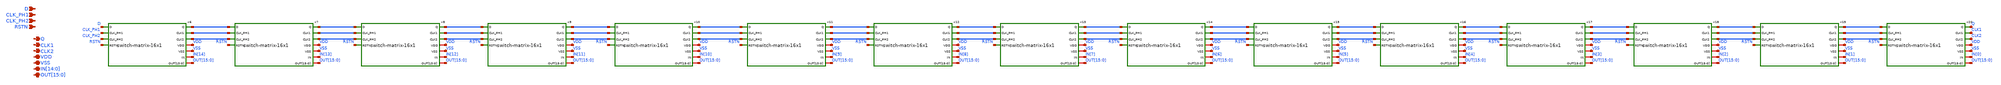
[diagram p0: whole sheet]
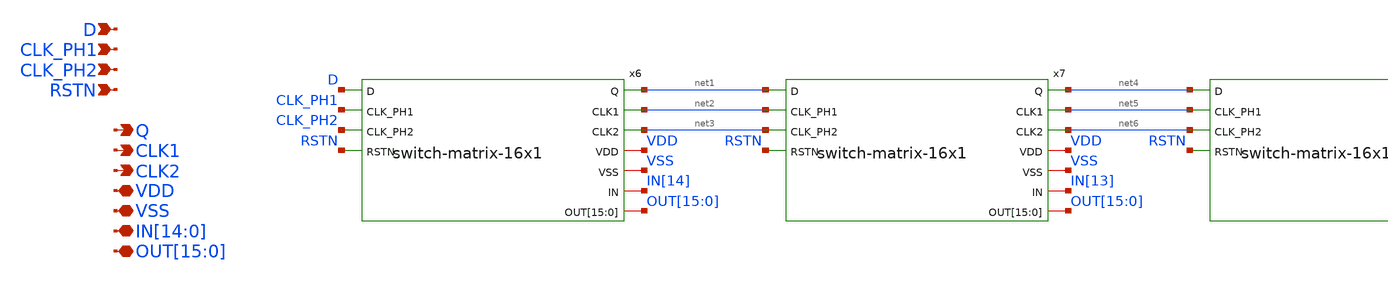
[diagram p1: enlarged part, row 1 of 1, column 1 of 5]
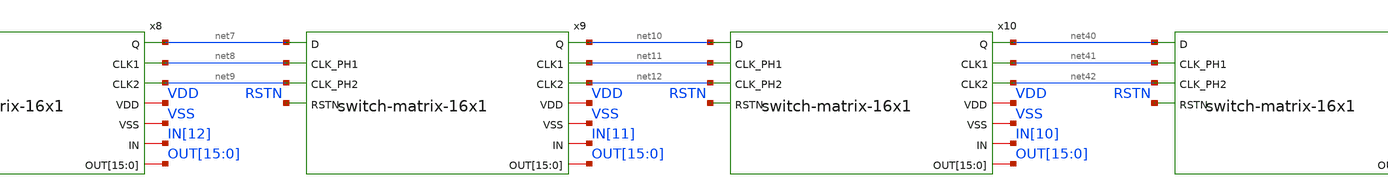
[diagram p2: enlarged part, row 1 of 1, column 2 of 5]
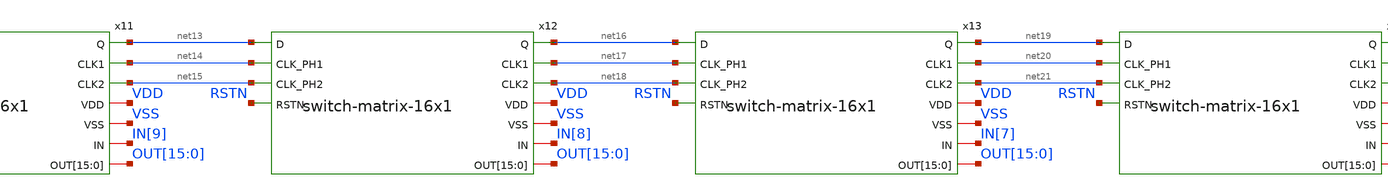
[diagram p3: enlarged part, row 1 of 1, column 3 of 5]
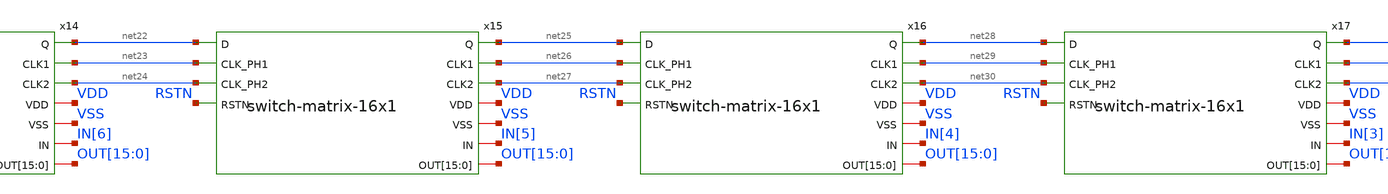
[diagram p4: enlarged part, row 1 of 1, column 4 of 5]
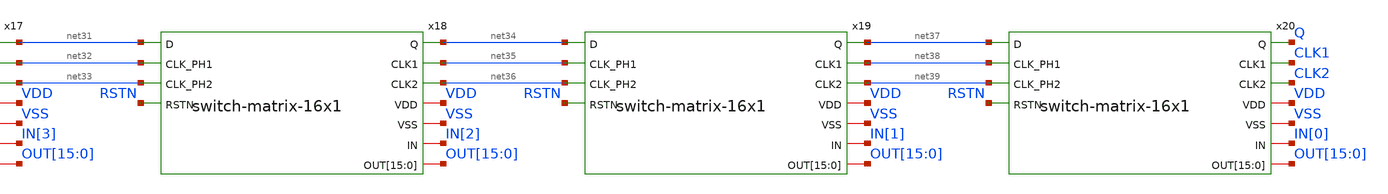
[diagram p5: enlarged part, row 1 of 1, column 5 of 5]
** sch_path: designs/libs/core_switch-matrix/switch-matrix-16x20/switch-matrix-16x20.sch
**.subckt switch-matrix-16x20 D CLK_PH1 CLK_PH2 RSTN VDD VSS
*+ IN[14],IN[13],IN[12],IN[11],IN[10],IN[9],IN[8],IN[7],IN[6],IN[5],IN[4],IN[3],IN[2],IN[1],IN[0]
*+ OUT[15],OUT[14],OUT[13],OUT[12],OUT[11],OUT[10],OUT[9],OUT[8],OUT[7],OUT[6],OUT[5],OUT[4],OUT[3],OUT[2],OUT[1],OUT[0] Q CLK1 CLK2
*.ipin D
*.ipin CLK_PH1
*.ipin CLK_PH2
*.ipin RSTN
*.iopin VDD
*.iopin VSS
*.iopin
*+ IN[14],IN[13],IN[12],IN[11],IN[10],IN[9],IN[8],IN[7],IN[6],IN[5],IN[4],IN[3],IN[2],IN[1],IN[0]
*.iopin
*+ OUT[15],OUT[14],OUT[13],OUT[12],OUT[11],OUT[10],OUT[9],OUT[8],OUT[7],OUT[6],OUT[5],OUT[4],OUT[3],OUT[2],OUT[1],OUT[0]
*.opin Q
*.opin CLK1
*.opin CLK2
x6 net1 net2 net3 VDD VSS IN[14] OUT[15] OUT[14] OUT[13] OUT[12] OUT[11] OUT[10] OUT[9] OUT[8]
+ OUT[7] OUT[6] OUT[5] OUT[4] OUT[3] OUT[2] OUT[1] OUT[0] D CLK_PH1 CLK_PH2 RSTN switch-matrix-16x1
x7 net4 net5 net6 VDD VSS IN[13] OUT[15] OUT[14] OUT[13] OUT[12] OUT[11] OUT[10] OUT[9] OUT[8]
+ OUT[7] OUT[6] OUT[5] OUT[4] OUT[3] OUT[2] OUT[1] OUT[0] net1 net2 net3 RSTN switch-matrix-16x1
x8 net7 net8 net9 VDD VSS IN[12] OUT[15] OUT[14] OUT[13] OUT[12] OUT[11] OUT[10] OUT[9] OUT[8]
+ OUT[7] OUT[6] OUT[5] OUT[4] OUT[3] OUT[2] OUT[1] OUT[0] net4 net5 net6 RSTN switch-matrix-16x1
x9 net10 net11 net12 VDD VSS IN[11] OUT[15] OUT[14] OUT[13] OUT[12] OUT[11] OUT[10] OUT[9] OUT[8]
+ OUT[7] OUT[6] OUT[5] OUT[4] OUT[3] OUT[2] OUT[1] OUT[0] net7 net8 net9 RSTN switch-matrix-16x1
x10 net40 net41 net42 VDD VSS IN[10] OUT[15] OUT[14] OUT[13] OUT[12] OUT[11] OUT[10] OUT[9] OUT[8]
+ OUT[7] OUT[6] OUT[5] OUT[4] OUT[3] OUT[2] OUT[1] OUT[0] net10 net11 net12 RSTN switch-matrix-16x1
x11 net13 net14 net15 VDD VSS IN[9] OUT[15] OUT[14] OUT[13] OUT[12] OUT[11] OUT[10] OUT[9] OUT[8]
+ OUT[7] OUT[6] OUT[5] OUT[4] OUT[3] OUT[2] OUT[1] OUT[0] net40 net41 net42 RSTN switch-matrix-16x1
x12 net16 net17 net18 VDD VSS IN[8] OUT[15] OUT[14] OUT[13] OUT[12] OUT[11] OUT[10] OUT[9] OUT[8]
+ OUT[7] OUT[6] OUT[5] OUT[4] OUT[3] OUT[2] OUT[1] OUT[0] net13 net14 net15 RSTN switch-matrix-16x1
x13 net19 net20 net21 VDD VSS IN[7] OUT[15] OUT[14] OUT[13] OUT[12] OUT[11] OUT[10] OUT[9] OUT[8]
+ OUT[7] OUT[6] OUT[5] OUT[4] OUT[3] OUT[2] OUT[1] OUT[0] net16 net17 net18 RSTN switch-matrix-16x1
x14 net22 net23 net24 VDD VSS IN[6] OUT[15] OUT[14] OUT[13] OUT[12] OUT[11] OUT[10] OUT[9] OUT[8]
+ OUT[7] OUT[6] OUT[5] OUT[4] OUT[3] OUT[2] OUT[1] OUT[0] net19 net20 net21 RSTN switch-matrix-16x1
x15 net25 net26 net27 VDD VSS IN[5] OUT[15] OUT[14] OUT[13] OUT[12] OUT[11] OUT[10] OUT[9] OUT[8]
+ OUT[7] OUT[6] OUT[5] OUT[4] OUT[3] OUT[2] OUT[1] OUT[0] net22 net23 net24 RSTN switch-matrix-16x1
x16 net28 net29 net30 VDD VSS IN[4] OUT[15] OUT[14] OUT[13] OUT[12] OUT[11] OUT[10] OUT[9] OUT[8]
+ OUT[7] OUT[6] OUT[5] OUT[4] OUT[3] OUT[2] OUT[1] OUT[0] net25 net26 net27 RSTN switch-matrix-16x1
x17 net31 net32 net33 VDD VSS IN[3] OUT[15] OUT[14] OUT[13] OUT[12] OUT[11] OUT[10] OUT[9] OUT[8]
+ OUT[7] OUT[6] OUT[5] OUT[4] OUT[3] OUT[2] OUT[1] OUT[0] net28 net29 net30 RSTN switch-matrix-16x1
x18 net34 net35 net36 VDD VSS IN[2] OUT[15] OUT[14] OUT[13] OUT[12] OUT[11] OUT[10] OUT[9] OUT[8]
+ OUT[7] OUT[6] OUT[5] OUT[4] OUT[3] OUT[2] OUT[1] OUT[0] net31 net32 net33 RSTN switch-matrix-16x1
x19 net37 net38 net39 VDD VSS IN[1] OUT[15] OUT[14] OUT[13] OUT[12] OUT[11] OUT[10] OUT[9] OUT[8]
+ OUT[7] OUT[6] OUT[5] OUT[4] OUT[3] OUT[2] OUT[1] OUT[0] net34 net35 net36 RSTN switch-matrix-16x1
x20 Q CLK1 CLK2 VDD VSS IN[0] OUT[15] OUT[14] OUT[13] OUT[12] OUT[11] OUT[10] OUT[9] OUT[8] OUT[7]
+ OUT[6] OUT[5] OUT[4] OUT[3] OUT[2] OUT[1] OUT[0] net37 net38 net39 RSTN switch-matrix-16x1
**.ends
.end
